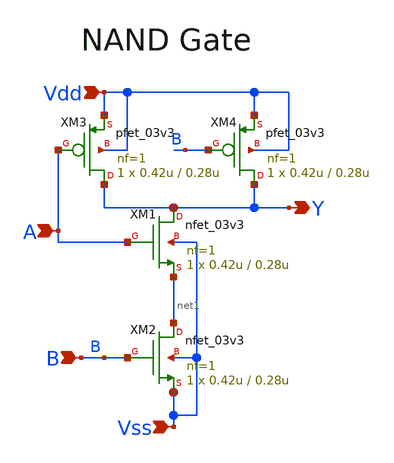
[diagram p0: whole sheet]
** sch_path: designs/libs/core_digital/schem/NAND2.sch
**.subckt NAND2 A B Vss Vdd Y
*.ipin A
*.ipin B
*.ipin Vss
*.ipin Vdd
*.opin Y
XM1 Y A net1 Vss nfet_03v3 L=0.28u W=0.42u nf=1 ad='int((nf+1)/2) * W/nf * 0.18u' as='int((nf+2)/2) * W/nf * 0.18u'
+ pd='2*int((nf+1)/2) * (W/nf + 0.18u)' ps='2*int((nf+2)/2) * (W/nf + 0.18u)' nrd='0.18u / W' nrs='0.18u / W'
+ sa=0 sb=0 sd=0 m=1
XM2 net1 B Vss Vss nfet_03v3 L=0.28u W=0.42u nf=1 ad='int((nf+1)/2) * W/nf * 0.18u' as='int((nf+2)/2) * W/nf * 0.18u'
+ pd='2*int((nf+1)/2) * (W/nf + 0.18u)' ps='2*int((nf+2)/2) * (W/nf + 0.18u)' nrd='0.18u / W' nrs='0.18u / W'
+ sa=0 sb=0 sd=0 m=1
XM3 Y A Vdd Vdd pfet_03v3 L=0.28u W=0.42u nf=1 ad='int((nf+1)/2) * W/nf * 0.18u' as='int((nf+2)/2) * W/nf * 0.18u'
+ pd='2*int((nf+1)/2) * (W/nf + 0.18u)' ps='2*int((nf+2)/2) * (W/nf + 0.18u)' nrd='0.18u / W' nrs='0.18u / W'
+ sa=0 sb=0 sd=0 m=1
XM4 Y B Vdd Vdd pfet_03v3 L=0.28u W=0.42u nf=1 ad='int((nf+1)/2) * W/nf * 0.18u' as='int((nf+2)/2) * W/nf * 0.18u'
+ pd='2*int((nf+1)/2) * (W/nf + 0.18u)' ps='2*int((nf+2)/2) * (W/nf + 0.18u)' nrd='0.18u / W' nrs='0.18u / W'
+ sa=0 sb=0 sd=0 m=1
**.ends
.end
